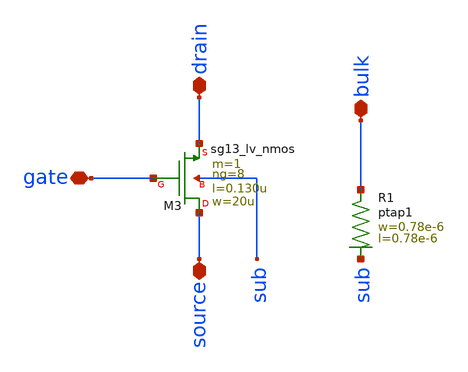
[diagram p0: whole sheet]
** sch_path: ts_pr_May2024/design_data/xschem/nmos8.sch
**.subckt nmos8 drain source bulk gate
*.iopin drain
*.iopin source
*.iopin bulk
*.iopin gate
XR1 bulk sub ptap1 R=262.8 w=0.78e-6 l=0.78e-6
XM3 source gate drain sub sg13_lv_nmos w=20u l=0.130u ng=8 m=1 mm_ok=1
**.ends
.end
